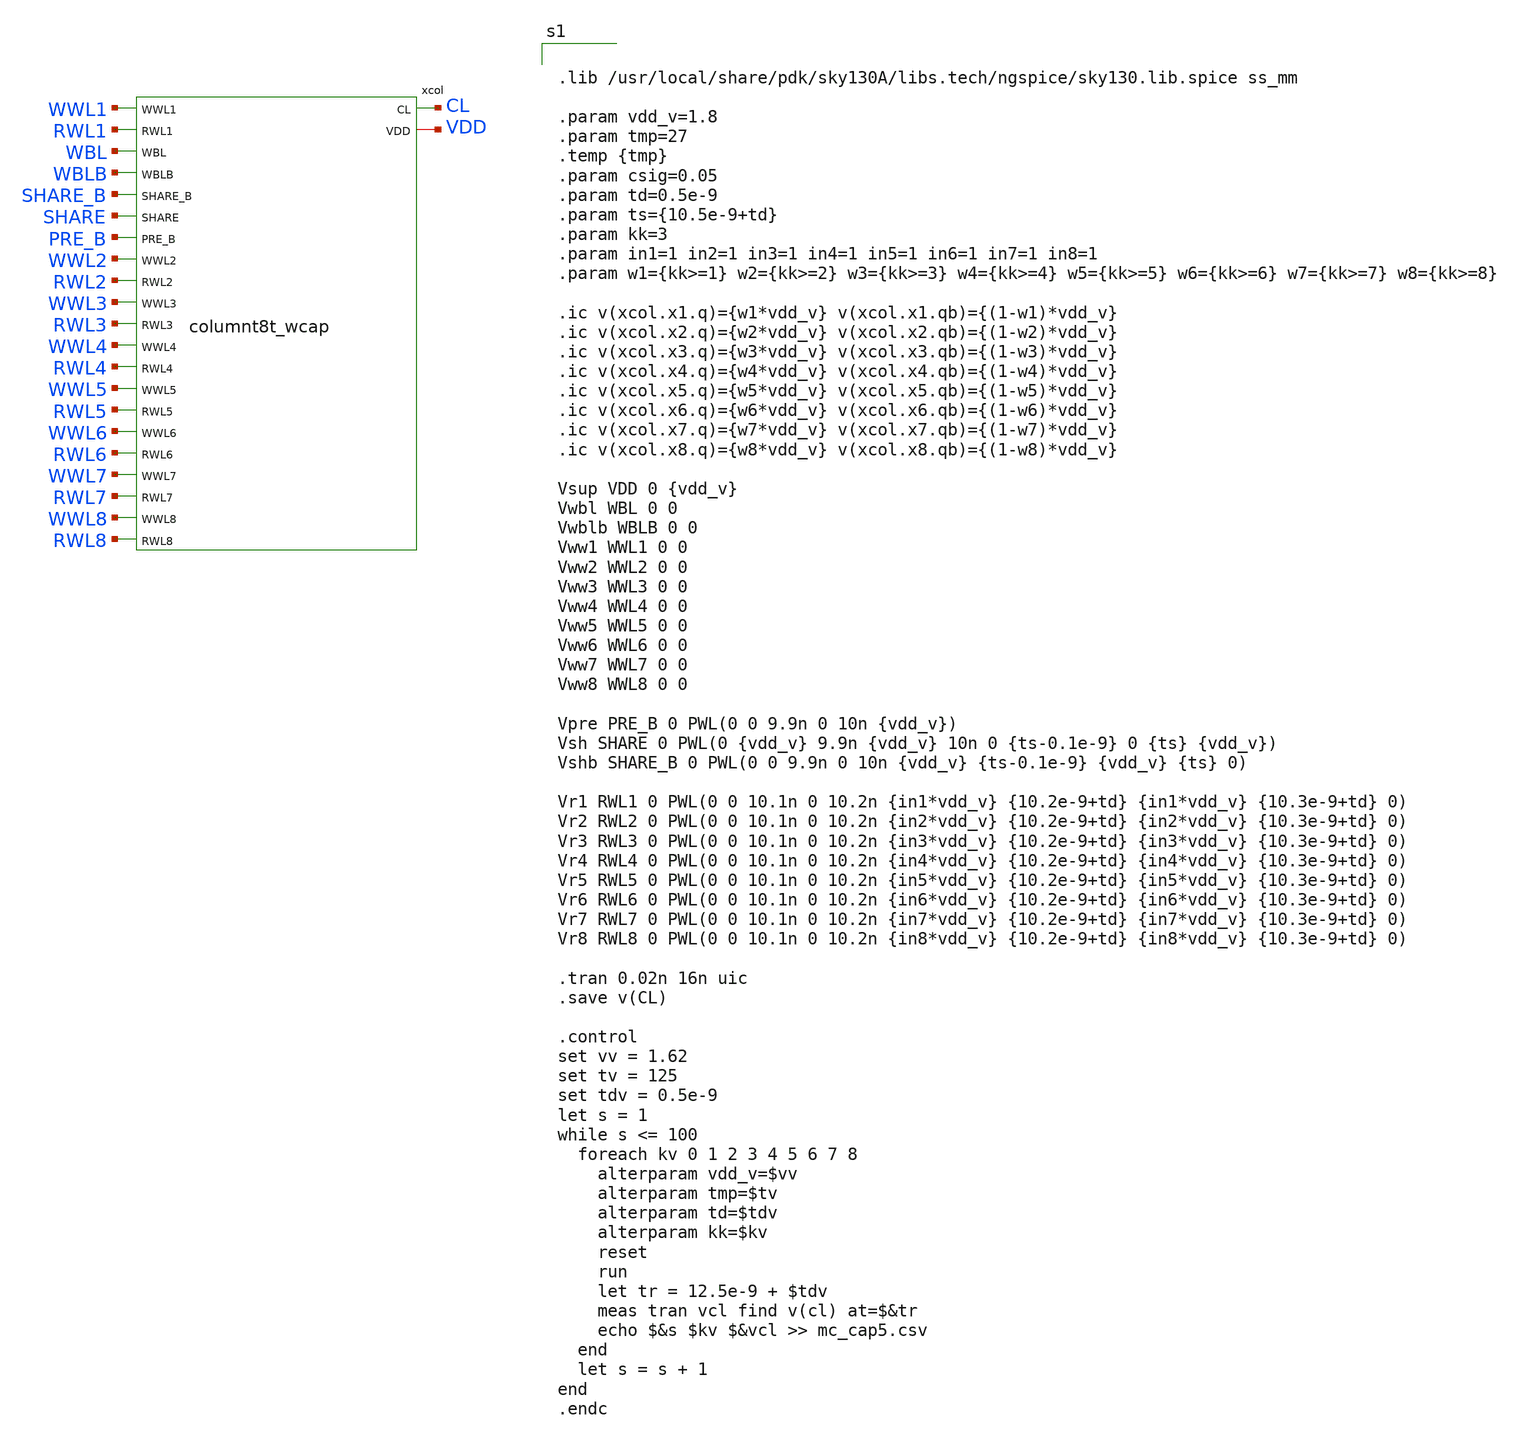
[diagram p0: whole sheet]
** sch_path: schematics/column_wcap.sch
**.subckt column_wcap
xcol CL VDD WWL1 RWL1 WBL WBLB SHARE_B SHARE PRE_B WWL2 RWL2 WWL3 RWL3 WWL4 RWL4 WWL5 RWL5 WWL6 RWL6
+ WWL7 RWL7 WWL8 RWL8 columnt8t_wcap
**** begin user architecture code


.lib /usr/local/share/pdk/sky130A/libs.tech/ngspice/sky130.lib.spice ss_mm

.param vdd_v=1.8
.param tmp=27
.temp {tmp}
.param csig=0.05
.param td=0.5e-9
.param ts={10.5e-9+td}
.param kk=3
.param in1=1 in2=1 in3=1 in4=1 in5=1 in6=1 in7=1 in8=1
.param w1={kk>=1} w2={kk>=2} w3={kk>=3} w4={kk>=4} w5={kk>=5} w6={kk>=6} w7={kk>=7} w8={kk>=8}

.ic v(xcol.x1.q)={w1*vdd_v} v(xcol.x1.qb)={(1-w1)*vdd_v}
.ic v(xcol.x2.q)={w2*vdd_v} v(xcol.x2.qb)={(1-w2)*vdd_v}
.ic v(xcol.x3.q)={w3*vdd_v} v(xcol.x3.qb)={(1-w3)*vdd_v}
.ic v(xcol.x4.q)={w4*vdd_v} v(xcol.x4.qb)={(1-w4)*vdd_v}
.ic v(xcol.x5.q)={w5*vdd_v} v(xcol.x5.qb)={(1-w5)*vdd_v}
.ic v(xcol.x6.q)={w6*vdd_v} v(xcol.x6.qb)={(1-w6)*vdd_v}
.ic v(xcol.x7.q)={w7*vdd_v} v(xcol.x7.qb)={(1-w7)*vdd_v}
.ic v(xcol.x8.q)={w8*vdd_v} v(xcol.x8.qb)={(1-w8)*vdd_v}

Vsup VDD 0 {vdd_v}
Vwbl WBL 0 0
Vwblb WBLB 0 0
Vww1 WWL1 0 0
Vww2 WWL2 0 0
Vww3 WWL3 0 0
Vww4 WWL4 0 0
Vww5 WWL5 0 0
Vww6 WWL6 0 0
Vww7 WWL7 0 0
Vww8 WWL8 0 0

Vpre PRE_B 0 PWL(0 0 9.9n 0 10n {vdd_v})
Vsh SHARE 0 PWL(0 {vdd_v} 9.9n {vdd_v} 10n 0 {ts-0.1e-9} 0 {ts} {vdd_v})
Vshb SHARE_B 0 PWL(0 0 9.9n 0 10n {vdd_v} {ts-0.1e-9} {vdd_v} {ts} 0)

Vr1 RWL1 0 PWL(0 0 10.1n 0 10.2n {in1*vdd_v} {10.2e-9+td} {in1*vdd_v} {10.3e-9+td} 0)
Vr2 RWL2 0 PWL(0 0 10.1n 0 10.2n {in2*vdd_v} {10.2e-9+td} {in2*vdd_v} {10.3e-9+td} 0)
Vr3 RWL3 0 PWL(0 0 10.1n 0 10.2n {in3*vdd_v} {10.2e-9+td} {in3*vdd_v} {10.3e-9+td} 0)
Vr4 RWL4 0 PWL(0 0 10.1n 0 10.2n {in4*vdd_v} {10.2e-9+td} {in4*vdd_v} {10.3e-9+td} 0)
Vr5 RWL5 0 PWL(0 0 10.1n 0 10.2n {in5*vdd_v} {10.2e-9+td} {in5*vdd_v} {10.3e-9+td} 0)
Vr6 RWL6 0 PWL(0 0 10.1n 0 10.2n {in6*vdd_v} {10.2e-9+td} {in6*vdd_v} {10.3e-9+td} 0)
Vr7 RWL7 0 PWL(0 0 10.1n 0 10.2n {in7*vdd_v} {10.2e-9+td} {in7*vdd_v} {10.3e-9+td} 0)
Vr8 RWL8 0 PWL(0 0 10.1n 0 10.2n {in8*vdd_v} {10.2e-9+td} {in8*vdd_v} {10.3e-9+td} 0)

.tran 0.02n 16n uic
.save v(CL)

.control
set vv = 1.62
set tv = 125
set tdv = 0.5e-9
let s = 1
while s <= 100
  foreach kv 0 1 2 3 4 5 6 7 8
    alterparam vdd_v=$vv
    alterparam tmp=$tv
    alterparam td=$tdv
    alterparam kk=$kv
    reset
    run
    let tr = 12.5e-9 + $tdv
    meas tran vcl find v(cl) at=$&tr
    echo $&s $kv $&vcl >> mc_cap5.csv
  end
  let s = s + 1
end
.endc


**** end user architecture code
**.ends

* expanding   symbol:  columnt8t_wcap.sym # of pins=23
** sym_path: schematics/columnt8t_wcap.sym
** sch_path: schematics/columnt8t_wcap.sch
.subckt columnt8t_wcap CL VDD WWL1 RWL1 WBL WBLB SHARE_B SHARE PRE_B WWL2 RWL2 WWL3 RWL3 WWL4 RWL4
+ WWL5 RWL5 WWL6 RWL6 WWL7 RWL7 WWL8 RWL8
*.iopin VDD
*.ipin WBL
*.ipin WBLB
*.ipin SHARE_B
*.ipin SHARE
*.ipin PRE_B
*.opin CL
*.ipin WWL1
*.ipin RWL1
*.ipin WWL2
*.ipin RWL2
*.ipin WWL3
*.ipin RWL3
*.ipin WWL4
*.ipin RWL4
*.ipin WWL5
*.ipin RWL5
*.ipin WWL6
*.ipin RWL6
*.ipin WWL7
*.ipin RWL7
*.ipin WWL8
*.ipin RWL8
x1 CL VDD WWL1 RWL1 WBL WBLB SHARE_B SHARE PRE_B sram_8t_wcap
x2 CL VDD WWL2 RWL2 WBL WBLB SHARE_B SHARE PRE_B sram_8t_wcap
x3 CL VDD WWL3 RWL3 WBL WBLB SHARE_B SHARE PRE_B sram_8t_wcap
x4 CL VDD WWL4 RWL4 WBL WBLB SHARE_B SHARE PRE_B sram_8t_wcap
x5 CL VDD WWL5 RWL5 WBL WBLB SHARE_B SHARE PRE_B sram_8t_wcap
x6 CL VDD WWL6 RWL6 WBL WBLB SHARE_B SHARE PRE_B sram_8t_wcap
x7 CL VDD WWL7 RWL7 WBL WBLB SHARE_B SHARE PRE_B sram_8t_wcap
x8 CL VDD WWL8 RWL8 WBL WBLB SHARE_B SHARE PRE_B sram_8t_wcap
.ends


* expanding   symbol:  sram_8t_wcap.sym # of pins=9
** sym_path: schematics/sram_8t_wcap.sym
** sch_path: schematics/sram_8t_wcap.sch
.subckt sram_8t_wcap CL VDD WWL RWL WBL WBLB SHARE_B SHARE PRE_B
*.ipin WBLB
*.ipin WBL
*.ipin RWL
*.ipin WWL
*.ipin VDD
*.ipin PRE_B
*.ipin CL
*.ipin SHARE
*.ipin SHARE_B
XM1 0 q qb 0 sky130_fd_pr__nfet_01v8 L=0.15 W=1 nf=1 ad='int((1 + 1)/2) * 1 / 1 * 0.29' as='int((1 + 2)/2) * 1 / 1 * 0.29'
+ pd='2*int((1 + 1)/2) * (1 / 1 + 0.29)' ps='2*int((1 + 2)/2) * (1 / 1 + 0.29)' nrd='0.29 / 1 ' nrs='0.29 / 1 '
+ sa=0 sb=0 sd=0 mult=1 m=1
XM2 VDD q qb VDD sky130_fd_pr__pfet_01v8 L=0.15 W=1 nf=1 ad='int((1 + 1)/2) * 1 / 1 * 0.29' as='int((1 + 2)/2) * 1 / 1 * 0.29'
+ pd='2*int((1 + 1)/2) * (1 / 1 + 0.29)' ps='2*int((1 + 2)/2) * (1 / 1 + 0.29)' nrd='0.29 / 1 ' nrs='0.29 / 1 '
+ sa=0 sb=0 sd=0 mult=1 m=1
XM3 q qb VDD VDD sky130_fd_pr__pfet_01v8 L=0.15 W=1 nf=1 ad='int((1 + 1)/2) * 1 / 1 * 0.29' as='int((1 + 2)/2) * 1 / 1 * 0.29'
+ pd='2*int((1 + 1)/2) * (1 / 1 + 0.29)' ps='2*int((1 + 2)/2) * (1 / 1 + 0.29)' nrd='0.29 / 1 ' nrs='0.29 / 1 '
+ sa=0 sb=0 sd=0 mult=1 m=1
XM4 q qb 0 0 sky130_fd_pr__nfet_01v8 L=0.15 W=1 nf=1 ad='int((1 + 1)/2) * 1 / 1 * 0.29' as='int((1 + 2)/2) * 1 / 1 * 0.29'
+ pd='2*int((1 + 1)/2) * (1 / 1 + 0.29)' ps='2*int((1 + 2)/2) * (1 / 1 + 0.29)' nrd='0.29 / 1 ' nrs='0.29 / 1 '
+ sa=0 sb=0 sd=0 mult=1 m=1
XM5 qb WWL WBLB 0 sky130_fd_pr__nfet_01v8 L=0.15 W=1 nf=1 ad='int((1 + 1)/2) * 1 / 1 * 0.29' as='int((1 + 2)/2) * 1 / 1 * 0.29'
+ pd='2*int((1 + 1)/2) * (1 / 1 + 0.29)' ps='2*int((1 + 2)/2) * (1 / 1 + 0.29)' nrd='0.29 / 1 ' nrs='0.29 / 1 '
+ sa=0 sb=0 sd=0 mult=1 m=1
XM6 WBL WWL q 0 sky130_fd_pr__nfet_01v8 L=0.15 W=1 nf=1 ad='int((1 + 1)/2) * 1 / 1 * 0.29' as='int((1 + 2)/2) * 1 / 1 * 0.29'
+ pd='2*int((1 + 1)/2) * (1 / 1 + 0.29)' ps='2*int((1 + 2)/2) * (1 / 1 + 0.29)' nrd='0.29 / 1 ' nrs='0.29 / 1 '
+ sa=0 sb=0 sd=0 mult=1 m=1
XM7 output q 0 0 sky130_fd_pr__nfet_01v8 L=0.15 W=1 nf=1 ad='int((1 + 1)/2) * 1 / 1 * 0.29' as='int((1 + 2)/2) * 1 / 1 * 0.29'
+ pd='2*int((1 + 1)/2) * (1 / 1 + 0.29)' ps='2*int((1 + 2)/2) * (1 / 1 + 0.29)' nrd='0.29 / 1 ' nrs='0.29 / 1 '
+ sa=0 sb=0 sd=0 mult=1 m=1
XM8 net1 RWL output 0 sky130_fd_pr__nfet_01v8 L=0.15 W=1 nf=1 ad='int((1 + 1)/2) * 1 / 1 * 0.29' as='int((1 + 2)/2) * 1 / 1 * 0.29'
+ pd='2*int((1 + 1)/2) * (1 / 1 + 0.29)' ps='2*int((1 + 2)/2) * (1 / 1 + 0.29)' nrd='0.29 / 1 ' nrs='0.29 / 1 '
+ sa=0 sb=0 sd=0 mult=1 m=1
C1 net1 0 {10f*(1+csig*agauss(0,1,1))} m=1
XM9 CL SHARE net1 0 sky130_fd_pr__nfet_01v8 L=0.15 W=1 nf=1 ad='int((1 + 1)/2) * 1 / 1 * 0.29' as='int((1 + 2)/2) * 1 / 1 * 0.29'
+ pd='2*int((1 + 1)/2) * (1 / 1 + 0.29)' ps='2*int((1 + 2)/2) * (1 / 1 + 0.29)' nrd='0.29 / 1 ' nrs='0.29 / 1 '
+ sa=0 sb=0 sd=0 mult=1 m=1
XM10 net1 PRE_B VDD VDD sky130_fd_pr__pfet_01v8 L=0.15 W=1 nf=1 ad='int((1 + 1)/2) * 1 / 1 * 0.29' as='int((1 + 2)/2) * 1 / 1 * 0.29'
+ pd='2*int((1 + 1)/2) * (1 / 1 + 0.29)' ps='2*int((1 + 2)/2) * (1 / 1 + 0.29)' nrd='0.29 / 1 ' nrs='0.29 / 1 '
+ sa=0 sb=0 sd=0 mult=1 m=1
XM11 CL SHARE_B net1 VDD sky130_fd_pr__pfet_01v8 L=0.15 W=1 nf=1 ad='int((1 + 1)/2) * 1 / 1 * 0.29' as='int((1 + 2)/2) * 1 / 1 * 0.29'
+ pd='2*int((1 + 1)/2) * (1 / 1 + 0.29)' ps='2*int((1 + 2)/2) * (1 / 1 + 0.29)' nrd='0.29 / 1 ' nrs='0.29 / 1 '
+ sa=0 sb=0 sd=0 mult=1 m=1
.ends

.end
